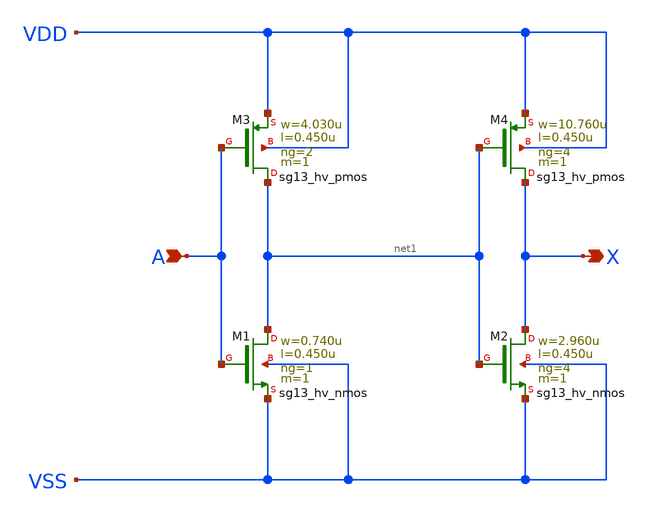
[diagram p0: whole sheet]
** sch_path: ihp-sg13g2/libs.ref/sg13g2_stdcell_hv/sch/xschem/sg13g2_hv_buf_4.sch
* Copyright 2023 IHP PDK Authors
* Licensed under the Apache License, Version 2.0 (the "License");
* you may not use this file except in compliance with the License.
* You may obtain a copy of the License at
* https://www.apache.org/licenses/LICENSE-2.0
* Unless required by applicable law or agreed to in writing, software
* distributed under the License is distributed on an "AS IS" BASIS,
* WITHOUT WARRANTIES OR CONDITIONS OF ANY KIND, either express or implied.
* See the License for the specific language governing permissions and
* limitations under the License.
**.subckt sg13g2_hv_buf_4 A X
*.ipin A
*.opin X
XM1 net1 A VSS VSS sg13_hv_nmos w=0.740u l=0.450u ng=1 m=1 mm_ok=1
XM2 X net1 VSS VSS sg13_hv_nmos w=2.960u l=0.450u ng=4 m=1 mm_ok=1
XM3 net1 A VDD VDD sg13_hv_pmos w=4.030u l=0.450u ng=2 m=1 mm_ok=1
XM4 X net1 VDD VDD sg13_hv_pmos w=10.760u l=0.450u ng=4 m=1 mm_ok=1
**.ends
.end
